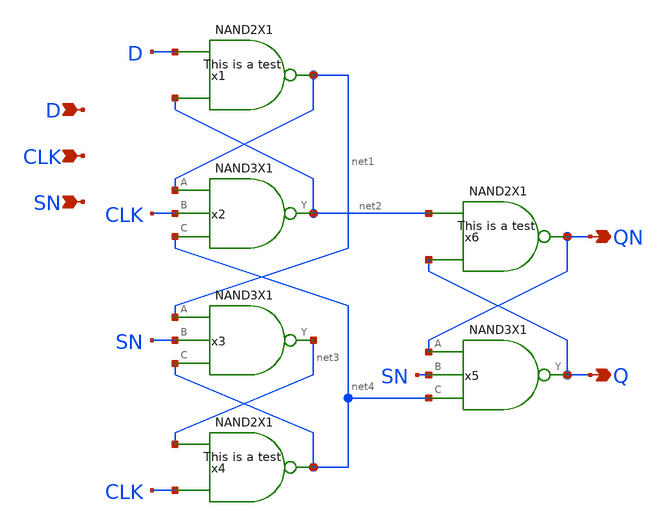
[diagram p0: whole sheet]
** sch_path: current/xschem/DFFSNX1.sch
**.subckt DFFSNX1 Q QN D CLK SN
*.opin Q
*.opin QN
*.ipin D
*.ipin CLK
*.ipin SN
x1 net1 D net2 VDD VSS NAND2X1
x2 net2 net1 CLK net4 VDD VSS NAND3X1
x3 net3 net1 SN net4 VDD VSS NAND3X1
x4 net4 net3 CLK VDD VSS NAND2X1
x5 Q QN SN net4 VDD VSS NAND3X1
x6 QN net2 Q VDD VSS NAND2X1
**.ends
.end
